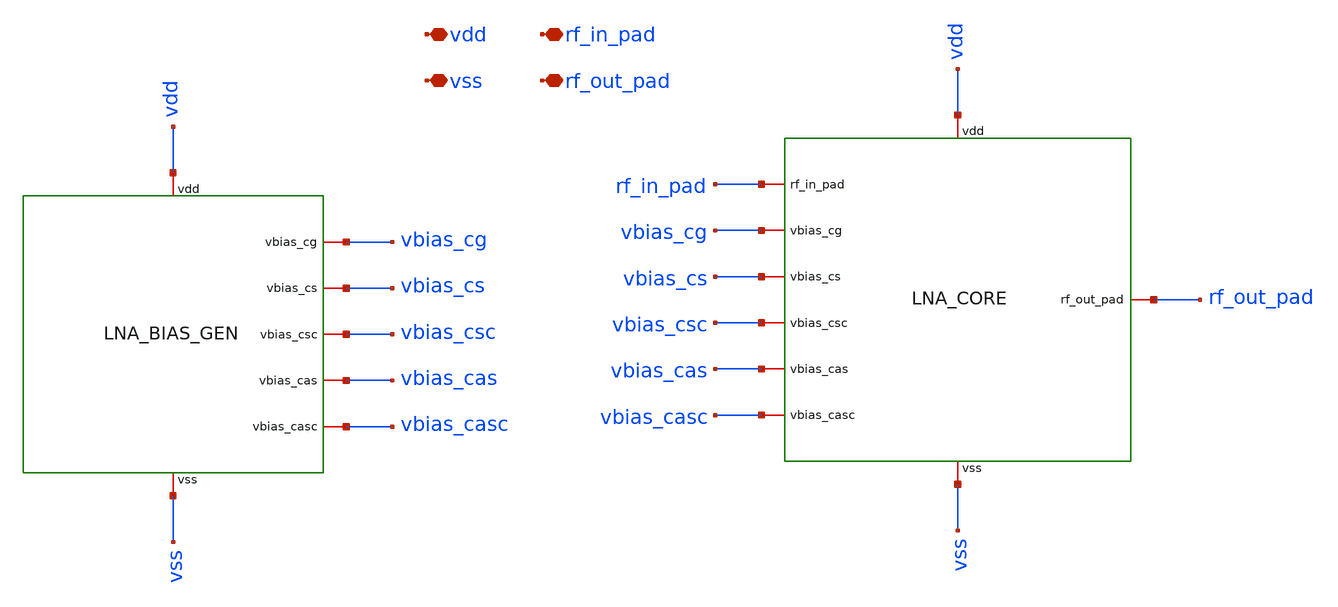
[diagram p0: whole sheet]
** sch_path: xschem/lna_v2/lna_top.sch
**.subckt lna_top vdd vss rf_in_pad rf_out_pad
*.iopin vdd
*.iopin vss
*.iopin rf_in_pad
*.iopin rf_out_pad
xbias vdd vbias_cg vbias_cs vbias_csc vbias_cas vbias_casc vss lna_bias_gen
x1 vdd rf_in_pad vbias_cg vbias_cs vbias_csc vbias_cas vbias_casc rf_out_pad vss lna_core
**.ends
.end
